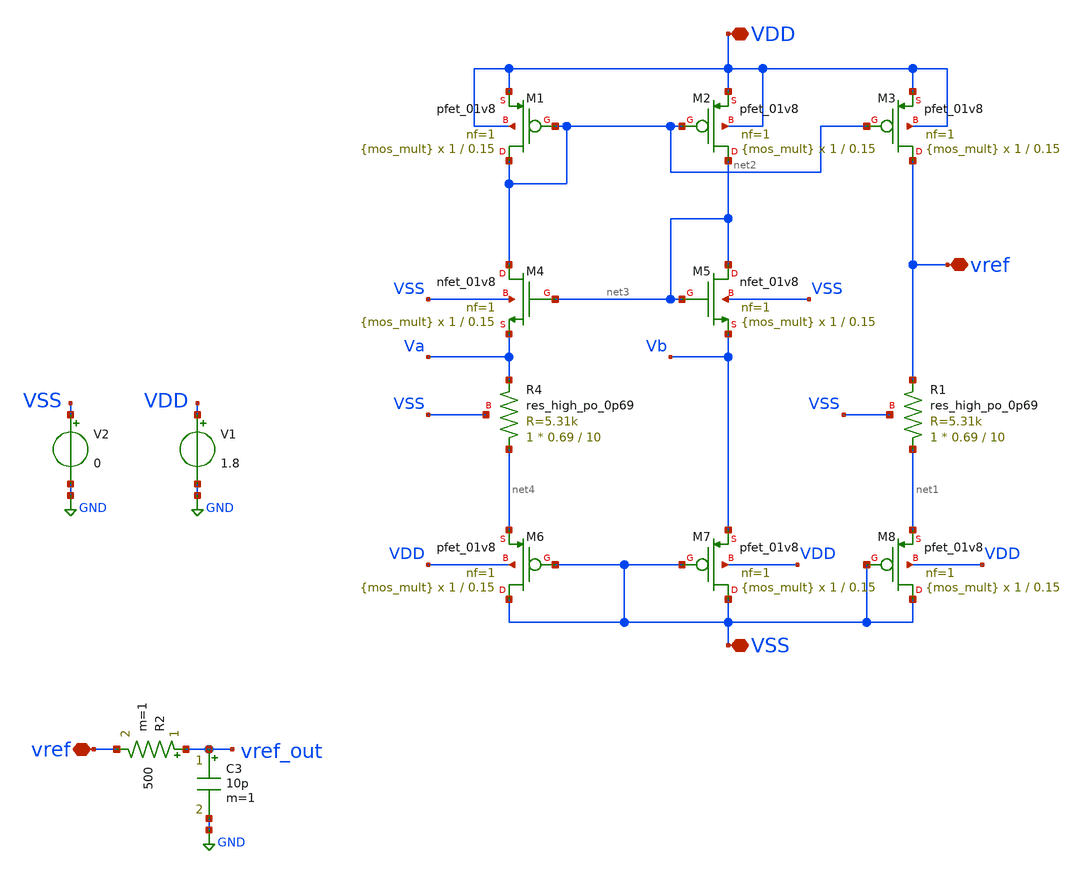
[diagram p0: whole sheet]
** sch_path: xschem/bandgap.sch
**.subckt bandgap VSS VDD vref vref
*.iopin VSS
*.iopin VDD
*.iopin vref
*.iopin vref
XM1 net2 net2 VDD VDD sky130_fd_pr__pfet_01v8 L=0.15 W=1 nf=1 ad='int((nf+1)/2) * W/nf * 0.29' as='int((nf+2)/2) * W/nf * 0.29'
+ pd='2*int((nf+1)/2) * (W/nf + 0.29)' ps='2*int((nf+2)/2) * (W/nf + 0.29)' nrd='0.29 / W' nrs='0.29 / W'
+ sa=0 sb=0 sd=0 mult={mos_mult} m={mos_mult}
XM2 net3 net2 VDD VDD sky130_fd_pr__pfet_01v8 L=0.15 W=1 nf=1 ad='int((nf+1)/2) * W/nf * 0.29' as='int((nf+2)/2) * W/nf * 0.29'
+ pd='2*int((nf+1)/2) * (W/nf + 0.29)' ps='2*int((nf+2)/2) * (W/nf + 0.29)' nrd='0.29 / W' nrs='0.29 / W'
+ sa=0 sb=0 sd=0 mult={mos_mult} m={mos_mult}
XM3 vref net2 VDD VDD sky130_fd_pr__pfet_01v8 L=0.15 W=1 nf=1 ad='int((nf+1)/2) * W/nf * 0.29' as='int((nf+2)/2) * W/nf * 0.29'
+ pd='2*int((nf+1)/2) * (W/nf + 0.29)' ps='2*int((nf+2)/2) * (W/nf + 0.29)' nrd='0.29 / W' nrs='0.29 / W'
+ sa=0 sb=0 sd=0 mult={mos_mult} m={mos_mult}
XM4 net2 net3 Va VSS sky130_fd_pr__nfet_01v8 L=0.15 W=1 nf=1 ad='int((nf+1)/2) * W/nf * 0.29' as='int((nf+2)/2) * W/nf * 0.29'
+ pd='2*int((nf+1)/2) * (W/nf + 0.29)' ps='2*int((nf+2)/2) * (W/nf + 0.29)' nrd='0.29 / W' nrs='0.29 / W'
+ sa=0 sb=0 sd=0 mult={mos_mult} m={mos_mult}
XM5 net3 net3 Vb VSS sky130_fd_pr__nfet_01v8 L=0.15 W=1 nf=1 ad='int((nf+1)/2) * W/nf * 0.29' as='int((nf+2)/2) * W/nf * 0.29'
+ pd='2*int((nf+1)/2) * (W/nf + 0.29)' ps='2*int((nf+2)/2) * (W/nf + 0.29)' nrd='0.29 / W' nrs='0.29 / W'
+ sa=0 sb=0 sd=0 mult={mos_mult} m={mos_mult}
XM6 VSS VSS net4 VDD sky130_fd_pr__pfet_01v8 L=0.15 W=1 nf=1 ad='int((nf+1)/2) * W/nf * 0.29' as='int((nf+2)/2) * W/nf * 0.29'
+ pd='2*int((nf+1)/2) * (W/nf + 0.29)' ps='2*int((nf+2)/2) * (W/nf + 0.29)' nrd='0.29 / W' nrs='0.29 / W'
+ sa=0 sb=0 sd=0 mult={mos_mult} m={mos_mult}
XM7 VSS VSS Vb VDD sky130_fd_pr__pfet_01v8 L=0.15 W=1 nf=1 ad='int((nf+1)/2) * W/nf * 0.29' as='int((nf+2)/2) * W/nf * 0.29'
+ pd='2*int((nf+1)/2) * (W/nf + 0.29)' ps='2*int((nf+2)/2) * (W/nf + 0.29)' nrd='0.29 / W' nrs='0.29 / W'
+ sa=0 sb=0 sd=0 mult={mos_mult} m={mos_mult}
XM8 VSS VSS net1 VDD sky130_fd_pr__pfet_01v8 L=0.15 W=1 nf=1 ad='int((nf+1)/2) * W/nf * 0.29' as='int((nf+2)/2) * W/nf * 0.29'
+ pd='2*int((nf+1)/2) * (W/nf + 0.29)' ps='2*int((nf+2)/2) * (W/nf + 0.29)' nrd='0.29 / W' nrs='0.29 / W'
+ sa=0 sb=0 sd=0 mult={mos_mult} m={mos_mult}
V1 VDD GND 1.8
V2 VSS GND 0
XR4 net4 Va VSS sky130_fd_pr__res_high_po_0p69 L=10 mult=1 m=1
XR1 net1 vref VSS sky130_fd_pr__res_high_po_0p69 L=10 mult=1 m=1
R2 vref_out vref 500 m=1
C3 vref_out GND 10p m=1
**** begin user architecture code

** opencircuitdesign pdks install
.lib $::SKYWATER_MODELS/sky130.lib.spice tt





*.option  METHOD = GEAR
*.param mc_mm_switch=0
.control
.param mos_mult = 20
let tempv = 10            ; create a vector vddc and assign 1.8
repeat 20
  set temp = $&tempv         ; alter the voltage V1 using vector vddc
  tran 500n 6u uic
  let tempv = tempv + 5   ; update vddc
  write bandgap.raw
  set appendwrite
  reset
end
.endc



**** end user architecture code
**.ends
.GLOBAL GND
.end
